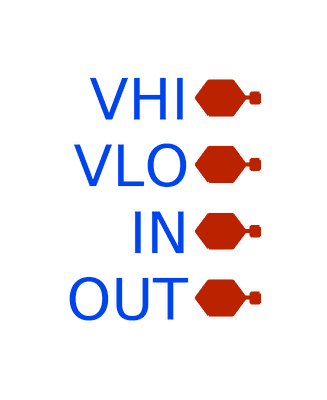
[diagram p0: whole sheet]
** sch_path: xschem/untitled-1.sch
**.subckt untitled-1 VHI VLO IN OUT
*.iopin VHI
*.iopin VLO
*.iopin IN
*.iopin OUT
**** begin user architecture code

X0 VHI a_4493_207# a_4493_207# VHI sky130_fd_pr__pfet_01v8 ad=2.9e+12p pd=2.058e+07u as=2.9e+12p
+ ps=2.058e+07u w=1e+07u l=2e+06u
X1 a_4493_207# VLO VLO VLO sky130_fd_pr__nfet_01v8 ad=1.45e+12p pd=1.058e+07u as=4.35e+12p
+ ps=3.174e+07u w=5e+06u l=2e+06u
X2 VLO VLO OUT VLO sky130_fd_pr__nfet_01v8 ad=0p pd=0u as=1.45e+12p ps=1.058e+07u w=5e+06u l=2e+06u
X3 a_5868_1637# a_5468_1540# OUT VHI sky130_fd_pr__pfet_01v8 ad=2.9e+12p pd=2.058e+07u as=2.9e+12p
+ ps=2.058e+07u w=1e+07u l=2e+06u
X4 OUT OUT VLO VLO sky130_fd_pr__nfet_01v8 ad=0p pd=0u as=0p ps=0u w=5e+06u l=2e+06u
X5 VLO IN a_4493_207# VLO sky130_fd_pr__nfet_01v8 ad=0p pd=0u as=0p ps=0u w=5e+06u l=2e+06u
X6 a_4493_207# a_4094_1540# a_4036_1637# VHI sky130_fd_pr__pfet_01v8 ad=0p pd=0u as=2.9e+12p
+ ps=2.058e+07u w=1e+07u l=2e+06u
X7 OUT a_4493_207# VHI VHI sky130_fd_pr__pfet_01v8 ad=0p pd=0u as=0p ps=0u w=1e+07u l=2e+06u


**** end user architecture code
**.ends
.end
